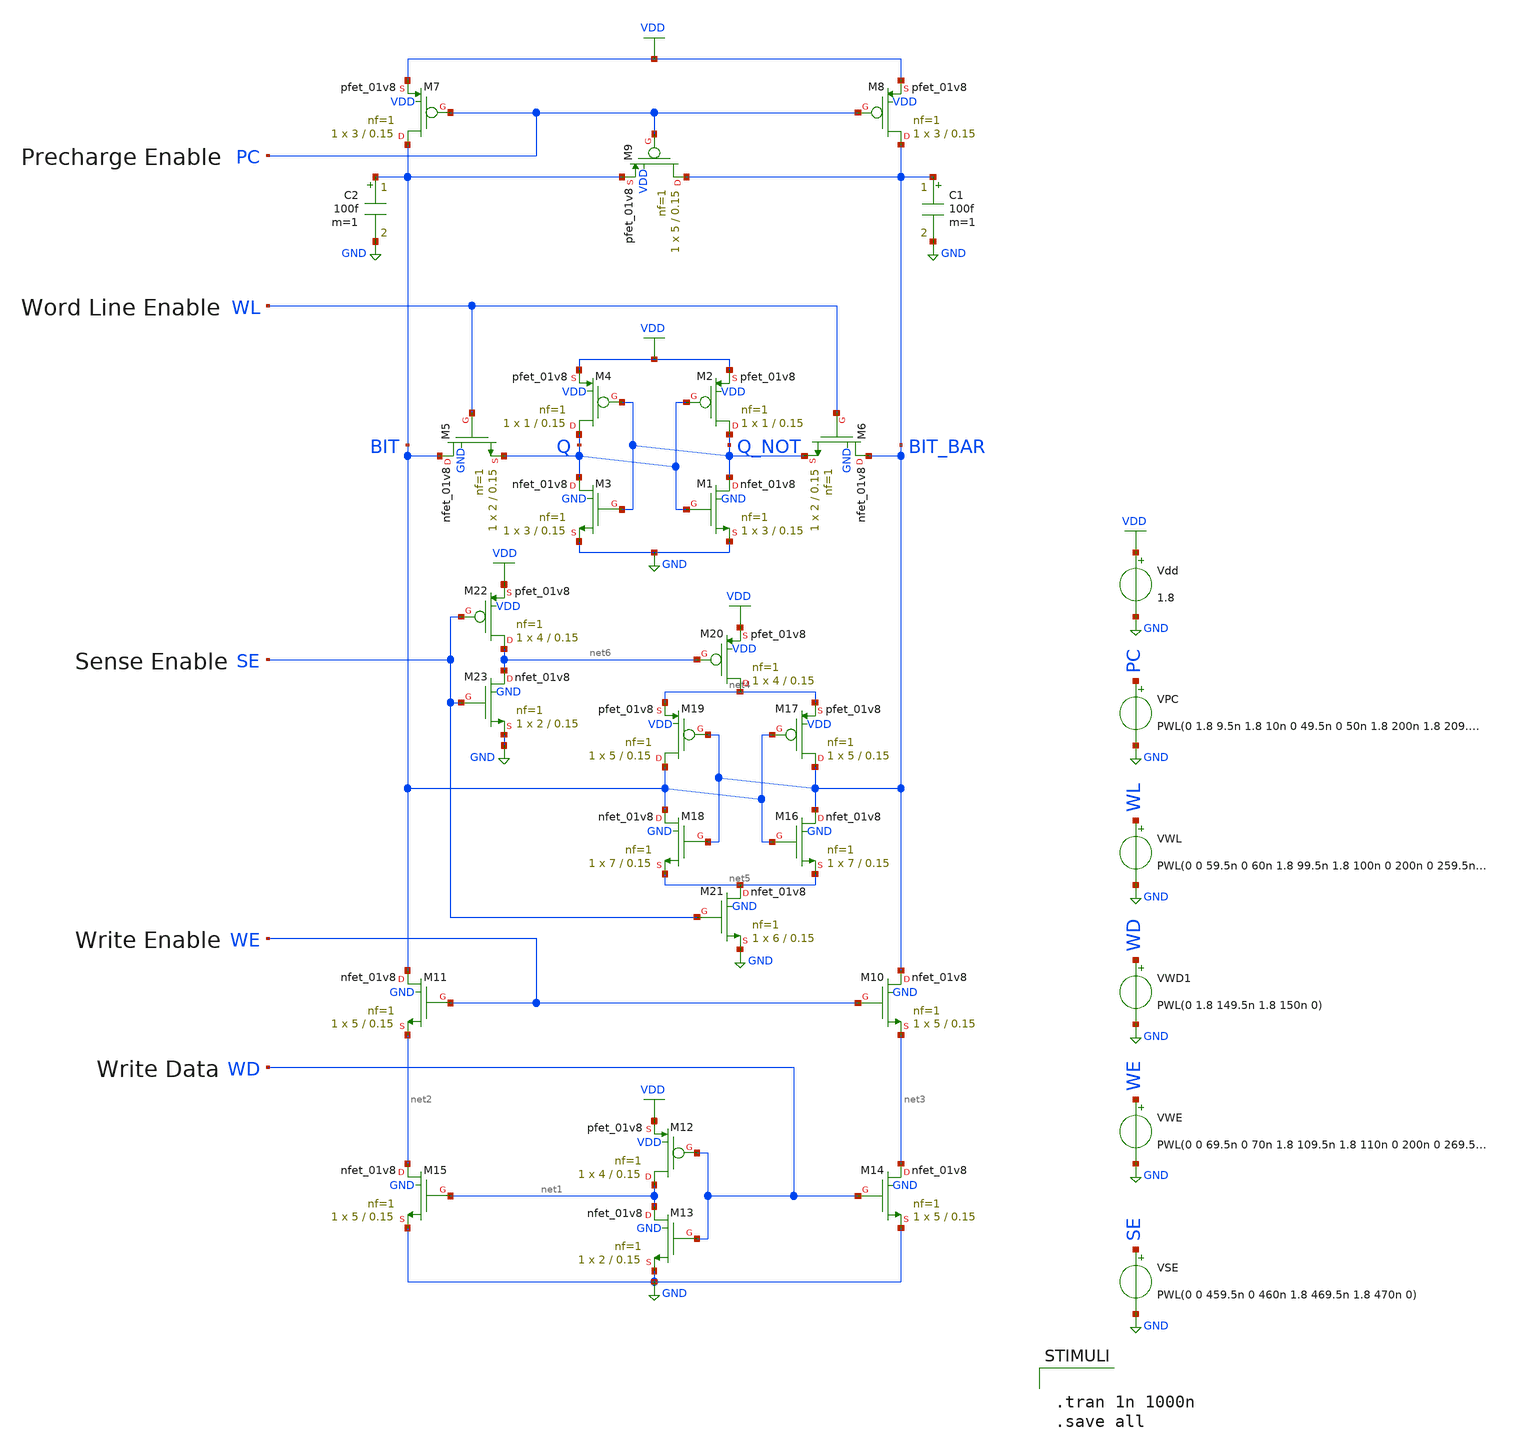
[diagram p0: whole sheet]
** sch_path: Examples/sram.sch
**.subckt sram
XM1 Q_NOT Q GND GND sky130_fd_pr__nfet_01v8 L=0.15 W=3 nf=1 ad='int((nf+1)/2) * W/nf * 0.29' as='int((nf+2)/2) * W/nf * 0.29'
+ pd='2*int((nf+1)/2) * (W/nf + 0.29)' ps='2*int((nf+2)/2) * (W/nf + 0.29)' nrd='0.29 / W' nrs='0.29 / W'
+ sa=0 sb=0 sd=0 mult=1 m=1
XM2 Q_NOT Q VDD VDD sky130_fd_pr__pfet_01v8 L=0.15 W=1 nf=1 ad='int((nf+1)/2) * W/nf * 0.29' as='int((nf+2)/2) * W/nf * 0.29'
+ pd='2*int((nf+1)/2) * (W/nf + 0.29)' ps='2*int((nf+2)/2) * (W/nf + 0.29)' nrd='0.29 / W' nrs='0.29 / W'
+ sa=0 sb=0 sd=0 mult=1 m=1
XM3 Q Q_NOT GND GND sky130_fd_pr__nfet_01v8 L=0.15 W=3 nf=1 ad='int((nf+1)/2) * W/nf * 0.29' as='int((nf+2)/2) * W/nf * 0.29'
+ pd='2*int((nf+1)/2) * (W/nf + 0.29)' ps='2*int((nf+2)/2) * (W/nf + 0.29)' nrd='0.29 / W' nrs='0.29 / W'
+ sa=0 sb=0 sd=0 mult=1 m=1
XM4 Q Q_NOT VDD VDD sky130_fd_pr__pfet_01v8 L=0.15 W=1 nf=1 ad='int((nf+1)/2) * W/nf * 0.29' as='int((nf+2)/2) * W/nf * 0.29'
+ pd='2*int((nf+1)/2) * (W/nf + 0.29)' ps='2*int((nf+2)/2) * (W/nf + 0.29)' nrd='0.29 / W' nrs='0.29 / W'
+ sa=0 sb=0 sd=0 mult=1 m=1
XM5 BIT WL Q GND sky130_fd_pr__nfet_01v8 L=0.15 W=2 nf=1 ad='int((nf+1)/2) * W/nf * 0.29' as='int((nf+2)/2) * W/nf * 0.29'
+ pd='2*int((nf+1)/2) * (W/nf + 0.29)' ps='2*int((nf+2)/2) * (W/nf + 0.29)' nrd='0.29 / W' nrs='0.29 / W'
+ sa=0 sb=0 sd=0 mult=1 m=1
XM6 BIT_BAR WL Q_NOT GND sky130_fd_pr__nfet_01v8 L=0.15 W=2 nf=1 ad='int((nf+1)/2) * W/nf * 0.29' as='int((nf+2)/2) * W/nf * 0.29'
+ pd='2*int((nf+1)/2) * (W/nf + 0.29)' ps='2*int((nf+2)/2) * (W/nf + 0.29)' nrd='0.29 / W' nrs='0.29 / W'
+ sa=0 sb=0 sd=0 mult=1 m=1
Vdd VDD GND 1.8
XM7 BIT PC VDD VDD sky130_fd_pr__pfet_01v8 L=0.15 W=3 nf=1 ad='int((nf+1)/2) * W/nf * 0.29' as='int((nf+2)/2) * W/nf * 0.29'
+ pd='2*int((nf+1)/2) * (W/nf + 0.29)' ps='2*int((nf+2)/2) * (W/nf + 0.29)' nrd='0.29 / W' nrs='0.29 / W'
+ sa=0 sb=0 sd=0 mult=1 m=1
XM8 BIT_BAR PC VDD VDD sky130_fd_pr__pfet_01v8 L=0.15 W=3 nf=1 ad='int((nf+1)/2) * W/nf * 0.29' as='int((nf+2)/2) * W/nf * 0.29'
+ pd='2*int((nf+1)/2) * (W/nf + 0.29)' ps='2*int((nf+2)/2) * (W/nf + 0.29)' nrd='0.29 / W' nrs='0.29 / W'
+ sa=0 sb=0 sd=0 mult=1 m=1
XM9 BIT_BAR PC BIT VDD sky130_fd_pr__pfet_01v8 L=0.15 W=5 nf=1 ad='int((nf+1)/2) * W/nf * 0.29' as='int((nf+2)/2) * W/nf * 0.29'
+ pd='2*int((nf+1)/2) * (W/nf + 0.29)' ps='2*int((nf+2)/2) * (W/nf + 0.29)' nrd='0.29 / W' nrs='0.29 / W'
+ sa=0 sb=0 sd=0 mult=1 m=1
C1 BIT_BAR GND 100f m=1
C2 BIT GND 100f m=1
XM10 BIT_BAR WE net3 GND sky130_fd_pr__nfet_01v8 L=0.15 W=5 nf=1 ad='int((nf+1)/2) * W/nf * 0.29' as='int((nf+2)/2) * W/nf * 0.29'
+ pd='2*int((nf+1)/2) * (W/nf + 0.29)' ps='2*int((nf+2)/2) * (W/nf + 0.29)' nrd='0.29 / W' nrs='0.29 / W'
+ sa=0 sb=0 sd=0 mult=1 m=1
XM11 BIT WE net2 GND sky130_fd_pr__nfet_01v8 L=0.15 W=5 nf=1 ad='int((nf+1)/2) * W/nf * 0.29' as='int((nf+2)/2) * W/nf * 0.29'
+ pd='2*int((nf+1)/2) * (W/nf + 0.29)' ps='2*int((nf+2)/2) * (W/nf + 0.29)' nrd='0.29 / W' nrs='0.29 / W'
+ sa=0 sb=0 sd=0 mult=1 m=1
XM12 net1 WD VDD VDD sky130_fd_pr__pfet_01v8 L=0.15 W=4 nf=1 ad='int((nf+1)/2) * W/nf * 0.29' as='int((nf+2)/2) * W/nf * 0.29'
+ pd='2*int((nf+1)/2) * (W/nf + 0.29)' ps='2*int((nf+2)/2) * (W/nf + 0.29)' nrd='0.29 / W' nrs='0.29 / W'
+ sa=0 sb=0 sd=0 mult=1 m=1
XM13 net1 WD GND GND sky130_fd_pr__nfet_01v8 L=0.15 W=2 nf=1 ad='int((nf+1)/2) * W/nf * 0.29' as='int((nf+2)/2) * W/nf * 0.29'
+ pd='2*int((nf+1)/2) * (W/nf + 0.29)' ps='2*int((nf+2)/2) * (W/nf + 0.29)' nrd='0.29 / W' nrs='0.29 / W'
+ sa=0 sb=0 sd=0 mult=1 m=1
XM14 net3 WD GND GND sky130_fd_pr__nfet_01v8 L=0.15 W=5 nf=1 ad='int((nf+1)/2) * W/nf * 0.29' as='int((nf+2)/2) * W/nf * 0.29'
+ pd='2*int((nf+1)/2) * (W/nf + 0.29)' ps='2*int((nf+2)/2) * (W/nf + 0.29)' nrd='0.29 / W' nrs='0.29 / W'
+ sa=0 sb=0 sd=0 mult=1 m=1
XM15 net2 net1 GND GND sky130_fd_pr__nfet_01v8 L=0.15 W=5 nf=1 ad='int((nf+1)/2) * W/nf * 0.29' as='int((nf+2)/2) * W/nf * 0.29'
+ pd='2*int((nf+1)/2) * (W/nf + 0.29)' ps='2*int((nf+2)/2) * (W/nf + 0.29)' nrd='0.29 / W' nrs='0.29 / W'
+ sa=0 sb=0 sd=0 mult=1 m=1
VPC PC GND PWL(0 1.8 9.5n 1.8 10n 0 49.5n 0 50n 1.8 200n 1.8 209.5n 1.8 210n 0 249.5n 0 250n 1.8
+ 400n 1.8 409.5n 1.8 410n 0 449.5n 0 450n 1.8)
VWL WL GND PWL(0 0 59.5n 0 60n 1.8 99.5n 1.8 100n 0 200n 0 259.5n 0 260n 1.8 299.5n 1.8 300n 0 400n
+ 0 459.5n 0 460n 1.8 499.5n 1.8 500n 0)
VWD1 WD GND PWL(0 1.8 149.5n 1.8 150n 0)
VWE WE GND PWL(0 0 69.5n 0 70n 1.8 109.5n 1.8 110n 0 200n 0 269.5n 0 270n 1.8 309.5n 1.8 310n 0)
XM16 BIT_BAR BIT net5 GND sky130_fd_pr__nfet_01v8 L=0.15 W=7 nf=1 ad='int((nf+1)/2) * W/nf * 0.29' as='int((nf+2)/2) * W/nf * 0.29'
+ pd='2*int((nf+1)/2) * (W/nf + 0.29)' ps='2*int((nf+2)/2) * (W/nf + 0.29)' nrd='0.29 / W' nrs='0.29 / W'
+ sa=0 sb=0 sd=0 mult=1 m=1
XM17 BIT_BAR BIT net4 VDD sky130_fd_pr__pfet_01v8 L=0.15 W=5 nf=1 ad='int((nf+1)/2) * W/nf * 0.29' as='int((nf+2)/2) * W/nf * 0.29'
+ pd='2*int((nf+1)/2) * (W/nf + 0.29)' ps='2*int((nf+2)/2) * (W/nf + 0.29)' nrd='0.29 / W' nrs='0.29 / W'
+ sa=0 sb=0 sd=0 mult=1 m=1
XM18 BIT BIT_BAR net5 GND sky130_fd_pr__nfet_01v8 L=0.15 W=7 nf=1 ad='int((nf+1)/2) * W/nf * 0.29' as='int((nf+2)/2) * W/nf * 0.29'
+ pd='2*int((nf+1)/2) * (W/nf + 0.29)' ps='2*int((nf+2)/2) * (W/nf + 0.29)' nrd='0.29 / W' nrs='0.29 / W'
+ sa=0 sb=0 sd=0 mult=1 m=1
XM19 BIT BIT_BAR net4 VDD sky130_fd_pr__pfet_01v8 L=0.15 W=5 nf=1 ad='int((nf+1)/2) * W/nf * 0.29' as='int((nf+2)/2) * W/nf * 0.29'
+ pd='2*int((nf+1)/2) * (W/nf + 0.29)' ps='2*int((nf+2)/2) * (W/nf + 0.29)' nrd='0.29 / W' nrs='0.29 / W'
+ sa=0 sb=0 sd=0 mult=1 m=1
XM20 net4 net6 VDD VDD sky130_fd_pr__pfet_01v8 L=0.15 W=4 nf=1 ad='int((nf+1)/2) * W/nf * 0.29' as='int((nf+2)/2) * W/nf * 0.29'
+ pd='2*int((nf+1)/2) * (W/nf + 0.29)' ps='2*int((nf+2)/2) * (W/nf + 0.29)' nrd='0.29 / W' nrs='0.29 / W'
+ sa=0 sb=0 sd=0 mult=1 m=1
XM21 net5 SE GND GND sky130_fd_pr__nfet_01v8 L=0.15 W=6 nf=1 ad='int((nf+1)/2) * W/nf * 0.29' as='int((nf+2)/2) * W/nf * 0.29'
+ pd='2*int((nf+1)/2) * (W/nf + 0.29)' ps='2*int((nf+2)/2) * (W/nf + 0.29)' nrd='0.29 / W' nrs='0.29 / W'
+ sa=0 sb=0 sd=0 mult=1 m=1
XM22 net6 SE VDD VDD sky130_fd_pr__pfet_01v8 L=0.15 W=4 nf=1 ad='int((nf+1)/2) * W/nf * 0.29' as='int((nf+2)/2) * W/nf * 0.29'
+ pd='2*int((nf+1)/2) * (W/nf + 0.29)' ps='2*int((nf+2)/2) * (W/nf + 0.29)' nrd='0.29 / W' nrs='0.29 / W'
+ sa=0 sb=0 sd=0 mult=1 m=1
XM23 net6 SE GND GND sky130_fd_pr__nfet_01v8 L=0.15 W=2 nf=1 ad='int((nf+1)/2) * W/nf * 0.29' as='int((nf+2)/2) * W/nf * 0.29'
+ pd='2*int((nf+1)/2) * (W/nf + 0.29)' ps='2*int((nf+2)/2) * (W/nf + 0.29)' nrd='0.29 / W' nrs='0.29 / W'
+ sa=0 sb=0 sd=0 mult=1 m=1
VSE SE GND PWL(0 0 459.5n 0 460n 1.8 469.5n 1.8 470n 0)
**** begin user architecture code


.tran 1n 1000n
.save all



** opencircuitdesign pdks install
.lib $::SKYWATER_MODELS/sky130.lib.spice tt


**** end user architecture code
**.ends
.GLOBAL VDD
.GLOBAL GND
.end
